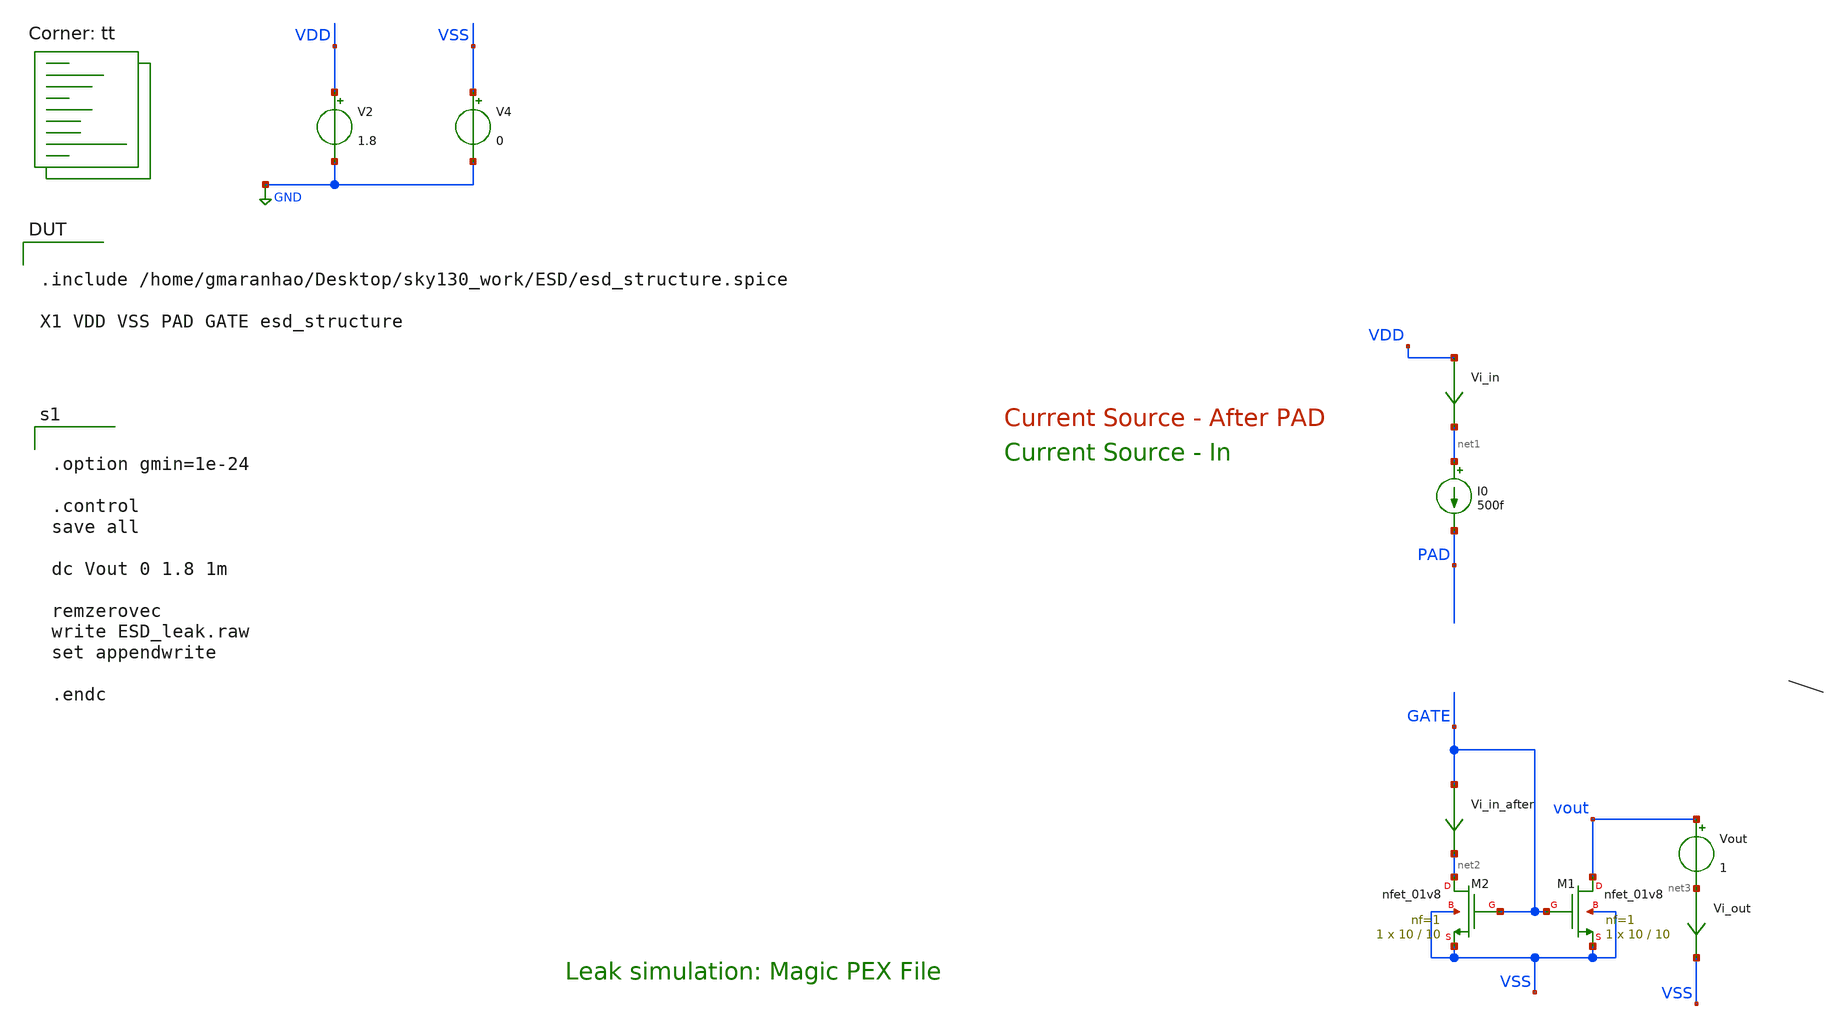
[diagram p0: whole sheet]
** sch_path: xschem/ESD/ESD_leak.sch
**.subckt ESD_leak
V2 VDD GND 1.8
V4 VSS GND 0
I0 net1 PAD 500f
Vi_in VDD net1 0
.save i(vi_in)
Vi_in_after GATE net2 0
.save i(vi_in_after)
Vi_out net3 VSS 0
.save i(vi_out)
Vout vout net3 1
XM1 vout GATE VSS VSS sky130_fd_pr__nfet_01v8 L=10 W=10 nf=1 ad='int((nf+1)/2) * W/nf * 0.29' as='int((nf+2)/2) * W/nf * 0.29'
+ pd='2*int((nf+1)/2) * (W/nf + 0.29)' ps='2*int((nf+2)/2) * (W/nf + 0.29)' nrd='0.29 / W' nrs='0.29 / W'
+ sa=0 sb=0 sd=0 mult=1 m=1
XM2 net2 GATE VSS VSS sky130_fd_pr__nfet_01v8 L=10 W=10 nf=1 ad='int((nf+1)/2) * W/nf * 0.29' as='int((nf+2)/2) * W/nf * 0.29'
+ pd='2*int((nf+1)/2) * (W/nf + 0.29)' ps='2*int((nf+2)/2) * (W/nf + 0.29)' nrd='0.29 / W' nrs='0.29 / W'
+ sa=0 sb=0 sd=0 mult=1 m=1
**** begin user architecture code


.option gmin=1e-24

.control
save all

dc Vout 0 1.8 1m

remzerovec
write ESD_leak.raw
set appendwrite

.endc



.include /home/gmaranhao/Desktop/sky130_work/ESD/esd_structure.spice

X1 VDD VSS PAD GATE esd_structure


.lib $::SKYWATER_MODELS/sky130.lib.spice tt
**** end user architecture code
**.ends
.GLOBAL GND
.end
